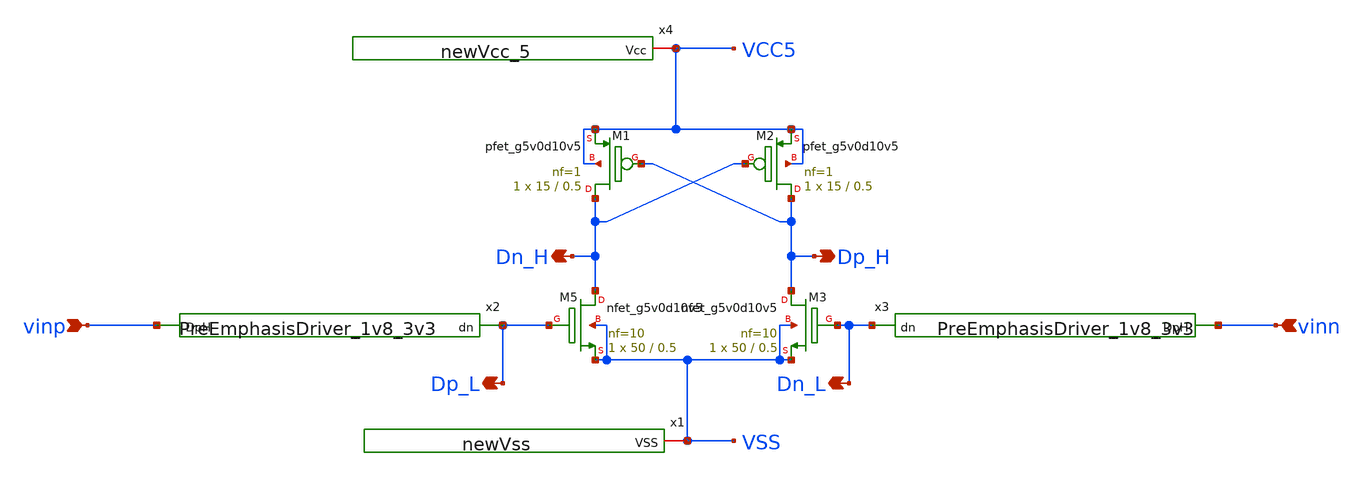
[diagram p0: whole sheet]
** sch_path: Git Files/Simulation Schematic/LevelShifter_5v.sch
**.subckt LevelShifter_5v Dp_H Dn_H vinp vinn Dp_L Dn_L
*.opin Dp_H
*.opin Dn_H
*.ipin vinp
*.ipin vinn
*.opin Dp_L
*.opin Dn_L
x1 VSS newVss
XM1 Dn_H Dp_H VCC5 VCC5 sky130_fd_pr__pfet_g5v0d10v5 L=0.5 W=15 nf=1 ad='int((nf+1)/2) * W/nf * 0.29'
+ as='int((nf+2)/2) * W/nf * 0.29' pd='2*int((nf+1)/2) * (W/nf + 0.29)' ps='2*int((nf+2)/2) * (W/nf + 0.29)'
+ nrd='0.29 / W' nrs='0.29 / W' sa=0 sb=0 sd=0 mult=1 m=1
XM2 Dp_H Dn_H VCC5 VCC5 sky130_fd_pr__pfet_g5v0d10v5 L=0.5 W=15 nf=1 ad='int((nf+1)/2) * W/nf * 0.29'
+ as='int((nf+2)/2) * W/nf * 0.29' pd='2*int((nf+1)/2) * (W/nf + 0.29)' ps='2*int((nf+2)/2) * (W/nf + 0.29)'
+ nrd='0.29 / W' nrs='0.29 / W' sa=0 sb=0 sd=0 mult=1 m=1
XM5 Dn_H Dp_L VSS VSS sky130_fd_pr__nfet_g5v0d10v5 L=0.5 W=50 nf=10 ad='int((nf+1)/2) * W/nf * 0.29'
+ as='int((nf+2)/2) * W/nf * 0.29' pd='2*int((nf+1)/2) * (W/nf + 0.29)' ps='2*int((nf+2)/2) * (W/nf + 0.29)'
+ nrd='0.29 / W' nrs='0.29 / W' sa=0 sb=0 sd=0 mult=1 m=1
XM3 Dp_H Dn_L VSS VSS sky130_fd_pr__nfet_g5v0d10v5 L=0.5 W=50 nf=10 ad='int((nf+1)/2) * W/nf * 0.29'
+ as='int((nf+2)/2) * W/nf * 0.29' pd='2*int((nf+1)/2) * (W/nf + 0.29)' ps='2*int((nf+2)/2) * (W/nf + 0.29)'
+ nrd='0.29 / W' nrs='0.29 / W' sa=0 sb=0 sd=0 mult=1 m=1
x2 Dp_L vinp PreEmphasisDriver_1v8_3v3
x3 Dn_L vinn PreEmphasisDriver_1v8_3v3
x4 VCC5 newVcc_5
**.ends
.end
